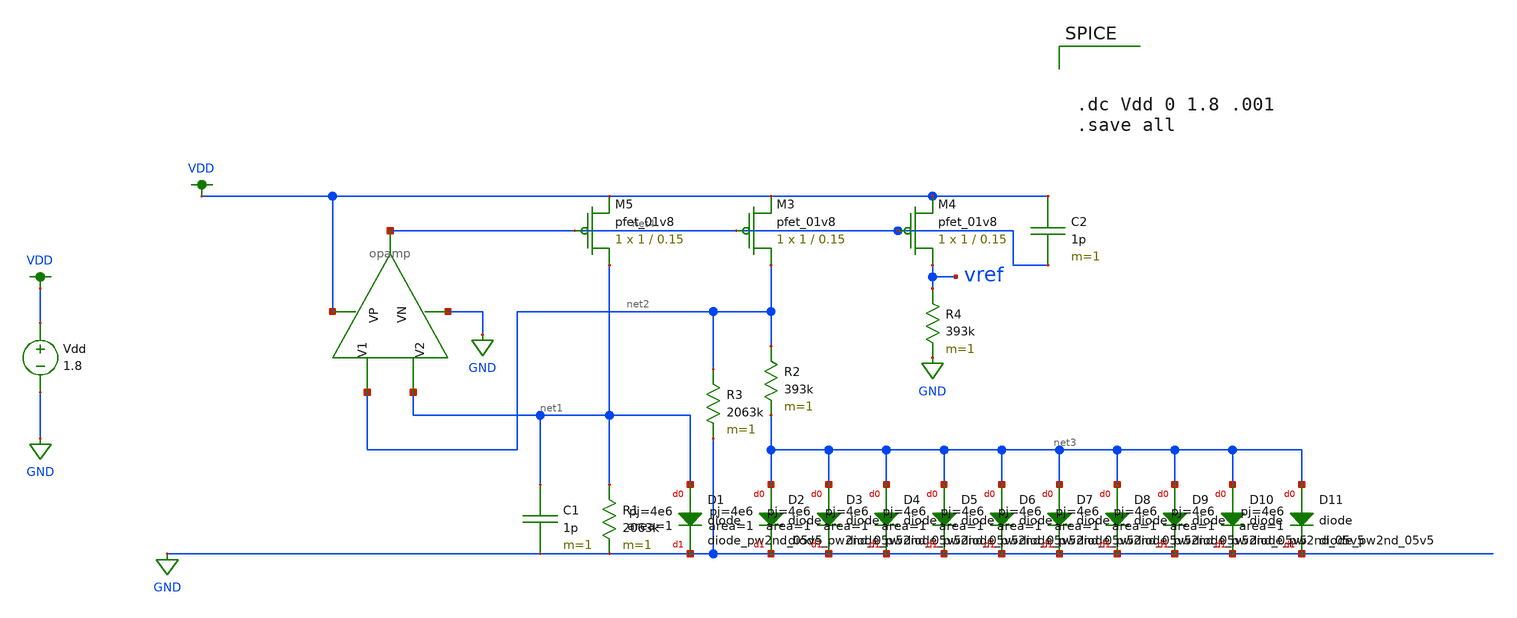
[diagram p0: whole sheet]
** sch_path: schematics/bandgap.sch
**.subckt bandgap
XD1 net1 GND sky130_fd_pr__diode_pw2nd_05v5 area=1 pj=4e6
XM4 vref net4 VDD VDD sky130_fd_pr__pfet_01v8 L=0.15 W=1 nf=1 ad='int((nf+1)/2) * W/nf * 0.29' as='int((nf+2)/2) * W/nf * 0.29'
+ pd='2*int((nf+1)/2) * (W/nf + 0.29)' ps='2*int((nf+2)/2) * (W/nf + 0.29)' nrd='0.29 / W' nrs='0.29 / W'
+ sa=0 sb=0 sd=0 mult=1 m=1
XM5 net1 net4 VDD VDD sky130_fd_pr__pfet_01v8 L=0.15 W=1 nf=1 ad='int((nf+1)/2) * W/nf * 0.29' as='int((nf+2)/2) * W/nf * 0.29'
+ pd='2*int((nf+1)/2) * (W/nf + 0.29)' ps='2*int((nf+2)/2) * (W/nf + 0.29)' nrd='0.29 / W' nrs='0.29 / W'
+ sa=0 sb=0 sd=0 mult=1 m=1
XM3 net2 net4 VDD VDD sky130_fd_pr__pfet_01v8 L=0.15 W=1 nf=1 ad='int((nf+1)/2) * W/nf * 0.29' as='int((nf+2)/2) * W/nf * 0.29'
+ pd='2*int((nf+1)/2) * (W/nf + 0.29)' ps='2*int((nf+2)/2) * (W/nf + 0.29)' nrd='0.29 / W' nrs='0.29 / W'
+ sa=0 sb=0 sd=0 mult=1 m=1
C1 net1 GND 1p m=1
R1 net1 GND 2063k m=1
XD2 net3 GND sky130_fd_pr__diode_pw2nd_05v5 area=1 pj=4e6
R2 net2 net3 393k m=1
XD3 net3 GND sky130_fd_pr__diode_pw2nd_05v5 area=1 pj=4e6
R3 net2 GND 2063k m=1
R4 vref GND 393k m=1
XD4 net3 GND sky130_fd_pr__diode_pw2nd_05v5 area=1 pj=4e6
XD5 net3 GND sky130_fd_pr__diode_pw2nd_05v5 area=1 pj=4e6
XD6 net3 GND sky130_fd_pr__diode_pw2nd_05v5 area=1 pj=4e6
XD7 net3 GND sky130_fd_pr__diode_pw2nd_05v5 area=1 pj=4e6
XD8 net3 GND sky130_fd_pr__diode_pw2nd_05v5 area=1 pj=4e6
XD9 net3 GND sky130_fd_pr__diode_pw2nd_05v5 area=1 pj=4e6
XD10 net3 GND sky130_fd_pr__diode_pw2nd_05v5 area=1 pj=4e6
XD11 net3 GND sky130_fd_pr__diode_pw2nd_05v5 area=1 pj=4e6
C2 VDD net4 1p m=1
Vdd VDD GND 1.8
X1 net2 net1 VDD GND net4 opamp
**** begin user architecture code

.option wnflag=1
.param MC_SWITCH=0.0
.lib ~/skywater/skywater-pdk/libraries/sky130_fd_pr_ngspice/latest/models/sky130.lib.spice tt




.dc Vdd 0 1.8 .001
.save all


**** end user architecture code
**.ends

* expanding   symbol:  /home/madvlsi/Desktop/MADVLSI_final/schematics/opamp.sym # of pins=5
** sym_path: schematics/opamp.sym
** sch_path: schematics/opamp.sch
.subckt opamp V1 V2 VP VN Vout
*.ipin V1
*.ipin V2
*.opin Vout
*.iopin VP
*.iopin VN
*.iopin VP
*.iopin VN
XM1 VN net6 net2 GND sky130_fd_pr__nfet_01v8 L=l W=w nf=1 ad='int((nf+1)/2) * W/nf * 0.29' as='int((nf+2)/2) * W/nf * 0.29'
+ pd='2*int((nf+1)/2) * (W/nf + 0.29)' ps='2*int((nf+2)/2) * (W/nf + 0.29)' nrd='0.29 / W' nrs='0.29 / W'
+ sa=0 sb=0 sd=0 mult=1 m=1
XM2 VP net3 net1 VDD sky130_fd_pr__pfet_01v8 L=l W=w nf=1 ad='int((nf+1)/2) * W/nf * 0.29' as='int((nf+2)/2) * W/nf * 0.29'
+ pd='2*int((nf+1)/2) * (W/nf + 0.29)' ps='2*int((nf+2)/2) * (W/nf + 0.29)' nrd='0.29 / W' nrs='0.29 / W'
+ sa=0 sb=0 sd=0 mult=1 m=1
XM3 net1 V2 Vd VDD sky130_fd_pr__pfet_01v8 L=l W=w nf=1 ad='int((nf+1)/2) * W/nf * 0.29' as='int((nf+2)/2) * W/nf * 0.29'
+ pd='2*int((nf+1)/2) * (W/nf + 0.29)' ps='2*int((nf+2)/2) * (W/nf + 0.29)' nrd='0.29 / W' nrs='0.29 / W'
+ sa=0 sb=0 sd=0 mult=1 m=1
XM4 Vc V1 net1 VDD sky130_fd_pr__pfet_01v8 L=l W=w nf=1 ad='int((nf+1)/2) * W/nf * 0.29' as='int((nf+2)/2) * W/nf * 0.29'
+ pd='2*int((nf+1)/2) * (W/nf + 0.29)' ps='2*int((nf+2)/2) * (W/nf + 0.29)' nrd='0.29 / W' nrs='0.29 / W'
+ sa=0 sb=0 sd=0 mult=1 m=1
XM5 Va V1 net2 GND sky130_fd_pr__nfet_01v8 L=l W=w nf=1 ad='int((nf+1)/2) * W/nf * 0.29' as='int((nf+2)/2) * W/nf * 0.29'
+ pd='2*int((nf+1)/2) * (W/nf + 0.29)' ps='2*int((nf+2)/2) * (W/nf + 0.29)' nrd='0.29 / W' nrs='0.29 / W'
+ sa=0 sb=0 sd=0 mult=1 m=1
XM6 net2 V2 Vb GND sky130_fd_pr__nfet_01v8 L=l W=w nf=1 ad='int((nf+1)/2) * W/nf * 0.29' as='int((nf+2)/2) * W/nf * 0.29'
+ pd='2*int((nf+1)/2) * (W/nf + 0.29)' ps='2*int((nf+2)/2) * (W/nf + 0.29)' nrd='0.29 / W' nrs='0.29 / W'
+ sa=0 sb=0 sd=0 mult=1 m=1
XM7 net3 net3 Va VDD sky130_fd_pr__pfet_01v8 L=l W=w nf=1 ad='int((nf+1)/2) * W/nf * 0.29' as='int((nf+2)/2) * W/nf * 0.29'
+ pd='2*int((nf+1)/2) * (W/nf + 0.29)' ps='2*int((nf+2)/2) * (W/nf + 0.29)' nrd='0.29 / W' nrs='0.29 / W'
+ sa=0 sb=0 sd=0 mult=1 m=1
XM8 net5 net5 Va VDD sky130_fd_pr__pfet_01v8 L=l W=w nf=1 ad='int((nf+1)/2) * W/nf * 0.29' as='int((nf+2)/2) * W/nf * 0.29'
+ pd='2*int((nf+1)/2) * (W/nf + 0.29)' ps='2*int((nf+2)/2) * (W/nf + 0.29)' nrd='0.29 / W' nrs='0.29 / W'
+ sa=0 sb=0 sd=0 mult=1 m=1
XM9 Vout net5 Vb VDD sky130_fd_pr__pfet_01v8 L=l W=w nf=1 ad='int((nf+1)/2) * W/nf * 0.29' as='int((nf+2)/2) * W/nf * 0.29'
+ pd='2*int((nf+1)/2) * (W/nf + 0.29)' ps='2*int((nf+2)/2) * (W/nf + 0.29)' nrd='0.29 / W' nrs='0.29 / W'
+ sa=0 sb=0 sd=0 mult=1 m=1
XM10 Va net3 VP VDD sky130_fd_pr__pfet_01v8 L=l W=w nf=1 ad='int((nf+1)/2) * W/nf * 0.29' as='int((nf+2)/2) * W/nf * 0.29'
+ pd='2*int((nf+1)/2) * (W/nf + 0.29)' ps='2*int((nf+2)/2) * (W/nf + 0.29)' nrd='0.29 / W' nrs='0.29 / W'
+ sa=0 sb=0 sd=0 mult=1 m=1
XM11 Vb net3 VP VDD sky130_fd_pr__pfet_01v8 L=l W=w nf=1 ad='int((nf+1)/2) * W/nf * 0.29' as='int((nf+2)/2) * W/nf * 0.29'
+ pd='2*int((nf+1)/2) * (W/nf + 0.29)' ps='2*int((nf+2)/2) * (W/nf + 0.29)' nrd='0.29 / W' nrs='0.29 / W'
+ sa=0 sb=0 sd=0 mult=1 m=1
XM12 net5 net5 Vc GND sky130_fd_pr__nfet_01v8 L=l W=w nf=1 ad='int((nf+1)/2) * W/nf * 0.29' as='int((nf+2)/2) * W/nf * 0.29'
+ pd='2*int((nf+1)/2) * (W/nf + 0.29)' ps='2*int((nf+2)/2) * (W/nf + 0.29)' nrd='0.29 / W' nrs='0.29 / W'
+ sa=0 sb=0 sd=0 mult=1 m=1
XM13 Vout net5 Vd GND sky130_fd_pr__nfet_01v8 L=l W=w nf=1 ad='int((nf+1)/2) * W/nf * 0.29' as='int((nf+2)/2) * W/nf * 0.29'
+ pd='2*int((nf+1)/2) * (W/nf + 0.29)' ps='2*int((nf+2)/2) * (W/nf + 0.29)' nrd='0.29 / W' nrs='0.29 / W'
+ sa=0 sb=0 sd=0 mult=1 m=1
XM14 Vc net6 VN GND sky130_fd_pr__nfet_01v8 L=l W=w nf=1 ad='int((nf+1)/2) * W/nf * 0.29' as='int((nf+2)/2) * W/nf * 0.29'
+ pd='2*int((nf+1)/2) * (W/nf + 0.29)' ps='2*int((nf+2)/2) * (W/nf + 0.29)' nrd='0.29 / W' nrs='0.29 / W'
+ sa=0 sb=0 sd=0 mult=1 m=1
XM15 Vd net6 VN GND sky130_fd_pr__nfet_01v8 L=l W=w nf=1 ad='int((nf+1)/2) * W/nf * 0.29' as='int((nf+2)/2) * W/nf * 0.29'
+ pd='2*int((nf+1)/2) * (W/nf + 0.29)' ps='2*int((nf+2)/2) * (W/nf + 0.29)' nrd='0.29 / W' nrs='0.29 / W'
+ sa=0 sb=0 sd=0 mult=1 m=1
XM16 net7 net6 net3 GND sky130_fd_pr__nfet_01v8 L=l W=w nf=1 ad='int((nf+1)/2) * W/nf * 0.29' as='int((nf+2)/2) * W/nf * 0.29'
+ pd='2*int((nf+1)/2) * (W/nf + 0.29)' ps='2*int((nf+2)/2) * (W/nf + 0.29)' nrd='0.29 / W' nrs='0.29 / W'
+ sa=0 sb=0 sd=0 mult=1 m=1
XM17 VN net6 net7 GND sky130_fd_pr__nfet_01v8 L=l W=w nf=1 ad='int((nf+1)/2) * W/nf * 0.29' as='int((nf+2)/2) * W/nf * 0.29'
+ pd='2*int((nf+1)/2) * (W/nf + 0.29)' ps='2*int((nf+2)/2) * (W/nf + 0.29)' nrd='0.29 / W' nrs='0.29 / W'
+ sa=0 sb=0 sd=0 mult=1 m=1
XM18 net7 net6 VP GND sky130_fd_pr__nfet_01v8 L=l W=w nf=1 ad='int((nf+1)/2) * W/nf * 0.29' as='int((nf+2)/2) * W/nf * 0.29'
+ pd='2*int((nf+1)/2) * (W/nf + 0.29)' ps='2*int((nf+2)/2) * (W/nf + 0.29)' nrd='0.29 / W' nrs='0.29 / W'
+ sa=0 sb=0 sd=0 mult=M m=M
XM19 net4 net3 net6 VDD sky130_fd_pr__pfet_01v8 L=l W=w nf=1 ad='int((nf+1)/2) * W/nf * 0.29' as='int((nf+2)/2) * W/nf * 0.29'
+ pd='2*int((nf+1)/2) * (W/nf + 0.29)' ps='2*int((nf+2)/2) * (W/nf + 0.29)' nrd='0.29 / W' nrs='0.29 / W'
+ sa=0 sb=0 sd=0 mult=1 m=1
XM20 VP net3 net4 VDD sky130_fd_pr__pfet_01v8 L=l W=w nf=1 ad='int((nf+1)/2) * W/nf * 0.29' as='int((nf+2)/2) * W/nf * 0.29'
+ pd='2*int((nf+1)/2) * (W/nf + 0.29)' ps='2*int((nf+2)/2) * (W/nf + 0.29)' nrd='0.29 / W' nrs='0.29 / W'
+ sa=0 sb=0 sd=0 mult=1 m=1
XM21 net4 net3 VN VDD sky130_fd_pr__pfet_01v8 L=l W=w nf=1 ad='int((nf+1)/2) * W/nf * 0.29' as='int((nf+2)/2) * W/nf * 0.29'
+ pd='2*int((nf+1)/2) * (W/nf + 0.29)' ps='2*int((nf+2)/2) * (W/nf + 0.29)' nrd='0.29 / W' nrs='0.29 / W'
+ sa=0 sb=0 sd=0 mult=M m=M
XM22 net6 net6 Vc GND sky130_fd_pr__nfet_01v8 L=l W=w nf=1 ad='int((nf+1)/2) * W/nf * 0.29' as='int((nf+2)/2) * W/nf * 0.29'
+ pd='2*int((nf+1)/2) * (W/nf + 0.29)' ps='2*int((nf+2)/2) * (W/nf + 0.29)' nrd='0.29 / W' nrs='0.29 / W'
+ sa=0 sb=0 sd=0 mult=1 m=1
**** begin user architecture code

.param M=8
.param w=3
.param l=0.6


**** end user architecture code
.ends

.GLOBAL VDD
.GLOBAL GND
.end
